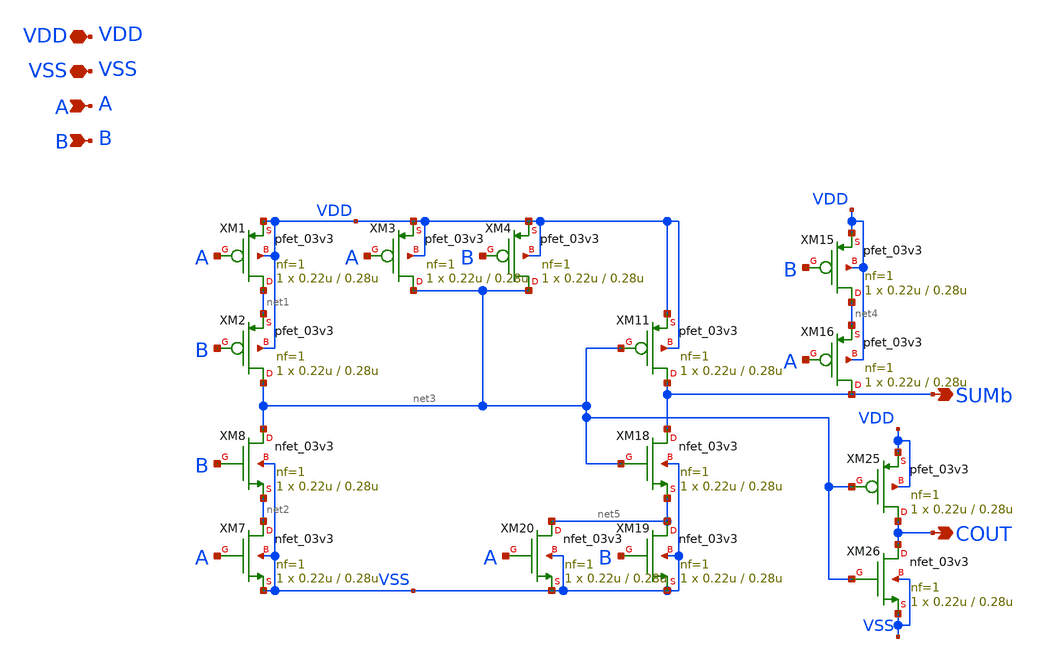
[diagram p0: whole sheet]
** sch_path: CAD4/full_adder_cin_0.sch
**.subckt full_adder_cin_0 VDD VSS A B SUMb COUT
*.iopin VDD
*.iopin VSS
*.ipin A
*.ipin B
*.opin SUMb
*.opin COUT
XM1 net1 A VDD VDD pfet_03v3 L=0.28u W=0.22u nf=1 ad='int((nf+1)/2) * W/nf * 0.18u' as='int((nf+2)/2) * W/nf * 0.18u'
+ pd='2*int((nf+1)/2) * (W/nf + 0.18u)' ps='2*int((nf+2)/2) * (W/nf + 0.18u)' nrd='0.18u / W' nrs='0.18u / W'
+ sa=0 sb=0 sd=0 m=1
XM2 net3 B net1 VDD pfet_03v3 L=0.28u W=0.22u nf=1 ad='int((nf+1)/2) * W/nf * 0.18u' as='int((nf+2)/2) * W/nf * 0.18u'
+ pd='2*int((nf+1)/2) * (W/nf + 0.18u)' ps='2*int((nf+2)/2) * (W/nf + 0.18u)' nrd='0.18u / W' nrs='0.18u / W'
+ sa=0 sb=0 sd=0 m=1
XM3 net3 A VDD VDD pfet_03v3 L=0.28u W=0.22u nf=1 ad='int((nf+1)/2) * W/nf * 0.18u' as='int((nf+2)/2) * W/nf * 0.18u'
+ pd='2*int((nf+1)/2) * (W/nf + 0.18u)' ps='2*int((nf+2)/2) * (W/nf + 0.18u)' nrd='0.18u / W' nrs='0.18u / W'
+ sa=0 sb=0 sd=0 m=1
XM4 net3 B VDD VDD pfet_03v3 L=0.28u W=0.22u nf=1 ad='int((nf+1)/2) * W/nf * 0.18u' as='int((nf+2)/2) * W/nf * 0.18u'
+ pd='2*int((nf+1)/2) * (W/nf + 0.18u)' ps='2*int((nf+2)/2) * (W/nf + 0.18u)' nrd='0.18u / W' nrs='0.18u / W'
+ sa=0 sb=0 sd=0 m=1
XM7 net2 A VSS VSS nfet_03v3 L=0.28u W=0.22u nf=1 ad='int((nf+1)/2) * W/nf * 0.18u' as='int((nf+2)/2) * W/nf * 0.18u'
+ pd='2*int((nf+1)/2) * (W/nf + 0.18u)' ps='2*int((nf+2)/2) * (W/nf + 0.18u)' nrd='0.18u / W' nrs='0.18u / W'
+ sa=0 sb=0 sd=0 m=1
XM8 net3 B net2 VSS nfet_03v3 L=0.28u W=0.22u nf=1 ad='int((nf+1)/2) * W/nf * 0.18u' as='int((nf+2)/2) * W/nf * 0.18u'
+ pd='2*int((nf+1)/2) * (W/nf + 0.18u)' ps='2*int((nf+2)/2) * (W/nf + 0.18u)' nrd='0.18u / W' nrs='0.18u / W'
+ sa=0 sb=0 sd=0 m=1
XM11 SUMb net3 VDD VDD pfet_03v3 L=0.28u W=0.22u nf=1 ad='int((nf+1)/2) * W/nf * 0.18u' as='int((nf+2)/2) * W/nf * 0.18u'
+ pd='2*int((nf+1)/2) * (W/nf + 0.18u)' ps='2*int((nf+2)/2) * (W/nf + 0.18u)' nrd='0.18u / W' nrs='0.18u / W'
+ sa=0 sb=0 sd=0 m=1
XM15 net4 B VDD VDD pfet_03v3 L=0.28u W=0.22u nf=1 ad='int((nf+1)/2) * W/nf * 0.18u' as='int((nf+2)/2) * W/nf * 0.18u'
+ pd='2*int((nf+1)/2) * (W/nf + 0.18u)' ps='2*int((nf+2)/2) * (W/nf + 0.18u)' nrd='0.18u / W' nrs='0.18u / W'
+ sa=0 sb=0 sd=0 m=1
XM16 SUMb A net4 VDD pfet_03v3 L=0.28u W=0.22u nf=1 ad='int((nf+1)/2) * W/nf * 0.18u' as='int((nf+2)/2) * W/nf * 0.18u'
+ pd='2*int((nf+1)/2) * (W/nf + 0.18u)' ps='2*int((nf+2)/2) * (W/nf + 0.18u)' nrd='0.18u / W' nrs='0.18u / W'
+ sa=0 sb=0 sd=0 m=1
XM18 SUMb net3 net5 VSS nfet_03v3 L=0.28u W=0.22u nf=1 ad='int((nf+1)/2) * W/nf * 0.18u' as='int((nf+2)/2) * W/nf * 0.18u'
+ pd='2*int((nf+1)/2) * (W/nf + 0.18u)' ps='2*int((nf+2)/2) * (W/nf + 0.18u)' nrd='0.18u / W' nrs='0.18u / W'
+ sa=0 sb=0 sd=0 m=1
XM19 net5 B VSS VSS nfet_03v3 L=0.28u W=0.22u nf=1 ad='int((nf+1)/2) * W/nf * 0.18u' as='int((nf+2)/2) * W/nf * 0.18u'
+ pd='2*int((nf+1)/2) * (W/nf + 0.18u)' ps='2*int((nf+2)/2) * (W/nf + 0.18u)' nrd='0.18u / W' nrs='0.18u / W'
+ sa=0 sb=0 sd=0 m=1
XM20 net5 A VSS VSS nfet_03v3 L=0.28u W=0.22u nf=1 ad='int((nf+1)/2) * W/nf * 0.18u' as='int((nf+2)/2) * W/nf * 0.18u'
+ pd='2*int((nf+1)/2) * (W/nf + 0.18u)' ps='2*int((nf+2)/2) * (W/nf + 0.18u)' nrd='0.18u / W' nrs='0.18u / W'
+ sa=0 sb=0 sd=0 m=1
XM25 COUT net3 VDD VDD pfet_03v3 L=0.28u W=0.22u nf=1 ad='int((nf+1)/2) * W/nf * 0.18u' as='int((nf+2)/2) * W/nf * 0.18u'
+ pd='2*int((nf+1)/2) * (W/nf + 0.18u)' ps='2*int((nf+2)/2) * (W/nf + 0.18u)' nrd='0.18u / W' nrs='0.18u / W'
+ sa=0 sb=0 sd=0 m=1
XM26 COUT net3 VSS VSS nfet_03v3 L=0.28u W=0.22u nf=1 ad='int((nf+1)/2) * W/nf * 0.18u' as='int((nf+2)/2) * W/nf * 0.18u'
+ pd='2*int((nf+1)/2) * (W/nf + 0.18u)' ps='2*int((nf+2)/2) * (W/nf + 0.18u)' nrd='0.18u / W' nrs='0.18u / W'
+ sa=0 sb=0 sd=0 m=1
**.ends
.end
